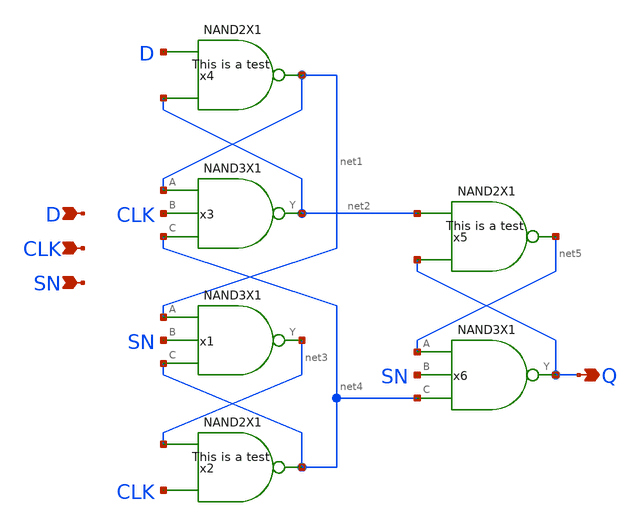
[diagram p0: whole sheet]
** sch_path: lib/xschem/DFFSNQX1.sch
**.subckt DFFSNQX1 Q D CLK SN
*.opin Q
*.ipin D
*.ipin CLK
*.ipin SN
x1 net3 net1 SN net4 VDD VSS NAND3X1
x2 net4 net3 CLK VDD VSS NAND2X1
x3 net2 net1 CLK net4 VDD VSS NAND3X1
x4 net1 D net2 VDD VSS NAND2X1
x5 net5 net2 Q VDD VSS NAND2X1
x6 Q net5 SN net4 VDD VSS NAND3X1
**.ends
.end
